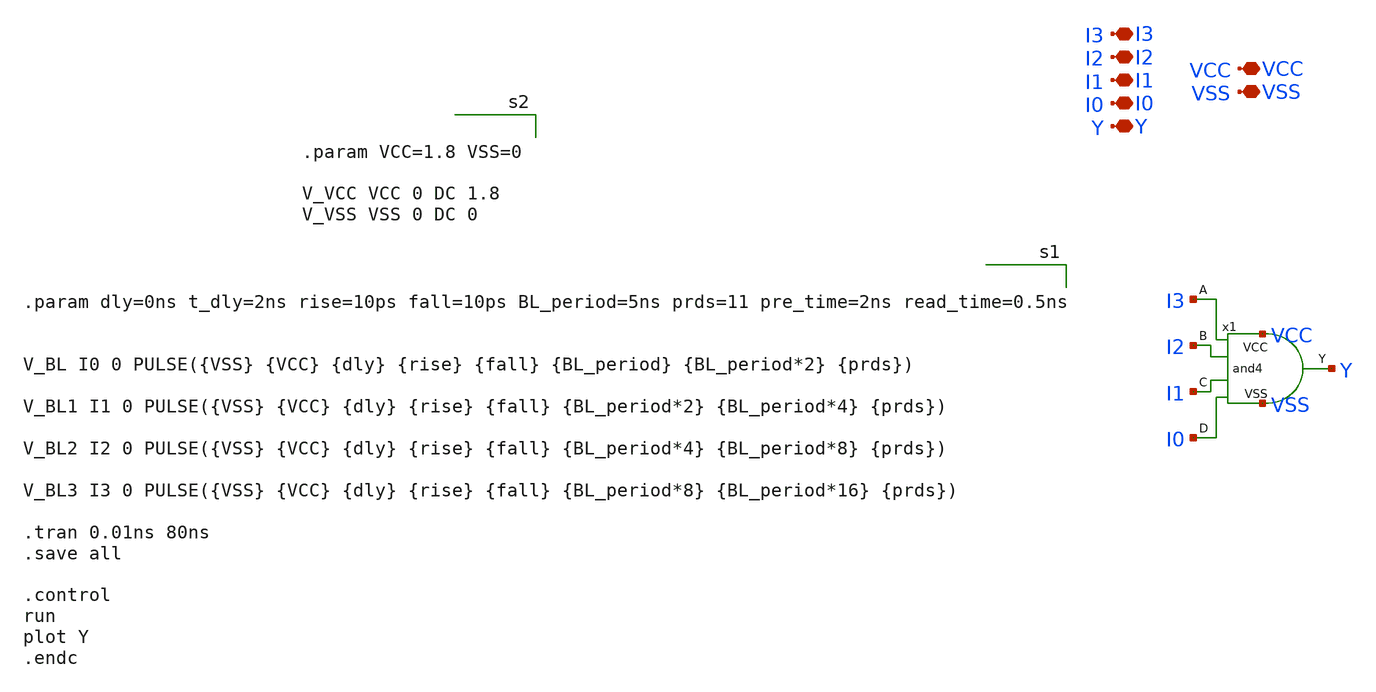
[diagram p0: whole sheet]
** sch_path: logic gates/logi_gate_test.sch
**.subckt logi_gate_test I2 I1 I0 VCC VSS Y I3
*.iopin I2
*.iopin I1
*.iopin I0
*.iopin VCC
*.iopin VSS
*.iopin Y
*.iopin I3
x1 VCC VSS I3 I2 I1 I0 Y and4
**** begin user architecture code


.param dly=0ns t_dly=2ns rise=10ps fall=10ps BL_period=5ns prds=11 pre_time=2ns read_time=0.5ns


V_BL I0 0 PULSE({VSS} {VCC} {dly} {rise} {fall} {BL_period} {BL_period*2} {prds})

V_BL1 I1 0 PULSE({VSS} {VCC} {dly} {rise} {fall} {BL_period*2} {BL_period*4} {prds})

V_BL2 I2 0 PULSE({VSS} {VCC} {dly} {rise} {fall} {BL_period*4} {BL_period*8} {prds})

V_BL3 I3 0 PULSE({VSS} {VCC} {dly} {rise} {fall} {BL_period*8} {BL_period*16} {prds})

.tran 0.01ns 80ns
.save all

.control
run
plot Y
.endc



** opencircuitdesign pdks install
.lib $::SKYWATER_MODELS/sky130.lib.spice tt



.param VCC=1.8 VSS=0

V_VCC VCC 0 DC 1.8
V_VSS VSS 0 DC 0


**** end user architecture code
**.ends

* expanding   symbol:  logic gates/and4.sym # of pins=7
** sym_path: logic gates/and4.sym
** sch_path: logic gates/and4.sch
.subckt and4 VCC VSS A B C D Y
*.iopin VSS
*.iopin Y
*.iopin A
*.iopin B
*.iopin C
*.iopin VCC
*.iopin D
x1 VCC Y net1 net2 VSS nor
x2 VCC net1 A B VSS nand
x3 VCC net2 C D VSS nand
.ends


* expanding   symbol:  logic gates/nor.sym # of pins=5
** sym_path: logic gates/nor.sym
** sch_path: logic gates/nor.sch
.subckt nor VCC Y A B VSS
*.iopin VCC
*.iopin VSS
*.iopin Y
*.iopin A
*.iopin B
XM2 Y B VSS VSS sky130_fd_pr__nfet_01v8 L=0.15 W=1 nf=1 ad='int((1 + 1)/2) * 1 / 1 * 0.29' as='int((1 + 2)/2) * 1 / 1 * 0.29'
+ pd='2*int((1 + 1)/2) * (1 / 1 + 0.29)' ps='2*int((1 + 2)/2) * (1 / 1 + 0.29)' nrd='0.29 / 1 ' nrs='0.29 / 1 '
+ sa=0 sb=0 sd=0 mult=1 m=1
XM11 Y B net1 VCC sky130_fd_pr__pfet_01v8 L=0.15 W=1 nf=1 ad='int((nf+1)/2) * W/nf * 0.29' as='int((nf+2)/2) * W/nf * 0.29'
+ pd='2*int((nf+1)/2) * (W/nf + 0.29)' ps='2*int((nf+2)/2) * (W/nf + 0.29)' nrd='0.29 / W' nrs='0.29 / W'
+ sa=0 sb=0 sd=0 mult=1 m=1
XM1 Y A VSS VSS sky130_fd_pr__nfet_01v8 L=0.15 W=1 nf=1 ad='int((1 + 1)/2) * 1 / 1 * 0.29' as='int((1 + 2)/2) * 1 / 1 * 0.29'
+ pd='2*int((1 + 1)/2) * (1 / 1 + 0.29)' ps='2*int((1 + 2)/2) * (1 / 1 + 0.29)' nrd='0.29 / 1 ' nrs='0.29 / 1 '
+ sa=0 sb=0 sd=0 mult=1 m=1
XM3 net1 A VCC VCC sky130_fd_pr__pfet_01v8 L=0.15 W=1 nf=1 ad='int((nf+1)/2) * W/nf * 0.29' as='int((nf+2)/2) * W/nf * 0.29'
+ pd='2*int((nf+1)/2) * (W/nf + 0.29)' ps='2*int((nf+2)/2) * (W/nf + 0.29)' nrd='0.29 / W' nrs='0.29 / W'
+ sa=0 sb=0 sd=0 mult=1 m=1
.ends


* expanding   symbol:  logic gates/nand.sym # of pins=5
** sym_path: logic gates/nand.sym
** sch_path: logic gates/nand.sch
.subckt nand VCC Y A B VSS
*.iopin VCC
*.iopin VSS
*.iopin Y
*.iopin A
*.iopin B
XM2 net1 B VSS VSS sky130_fd_pr__nfet_01v8 L=0.15 W=1 nf=1 ad='int((1 + 1)/2) * 1 / 1 * 0.29' as='int((1 + 2)/2) * 1 / 1 * 0.29'
+ pd='2*int((1 + 1)/2) * (1 / 1 + 0.29)' ps='2*int((1 + 2)/2) * (1 / 1 + 0.29)' nrd='0.29 / 1 ' nrs='0.29 / 1 '
+ sa=0 sb=0 sd=0 mult=1 m=1
XM11 Y A VCC VCC sky130_fd_pr__pfet_01v8 L=0.15 W=1 nf=1 ad='int((nf+1)/2) * W/nf * 0.29' as='int((nf+2)/2) * W/nf * 0.29'
+ pd='2*int((nf+1)/2) * (W/nf + 0.29)' ps='2*int((nf+2)/2) * (W/nf + 0.29)' nrd='0.29 / W' nrs='0.29 / W'
+ sa=0 sb=0 sd=0 mult=1 m=1
XM1 Y A net1 VSS sky130_fd_pr__nfet_01v8 L=0.15 W=1 nf=1 ad='int((1 + 1)/2) * 1 / 1 * 0.29' as='int((1 + 2)/2) * 1 / 1 * 0.29'
+ pd='2*int((1 + 1)/2) * (1 / 1 + 0.29)' ps='2*int((1 + 2)/2) * (1 / 1 + 0.29)' nrd='0.29 / 1 ' nrs='0.29 / 1 '
+ sa=0 sb=0 sd=0 mult=1 m=1
XM3 Y B VCC VCC sky130_fd_pr__pfet_01v8 L=0.15 W=1 nf=1 ad='int((nf+1)/2) * W/nf * 0.29' as='int((nf+2)/2) * W/nf * 0.29'
+ pd='2*int((nf+1)/2) * (W/nf + 0.29)' ps='2*int((nf+2)/2) * (W/nf + 0.29)' nrd='0.29 / W' nrs='0.29 / W'
+ sa=0 sb=0 sd=0 mult=1 m=1
.ends

.end
